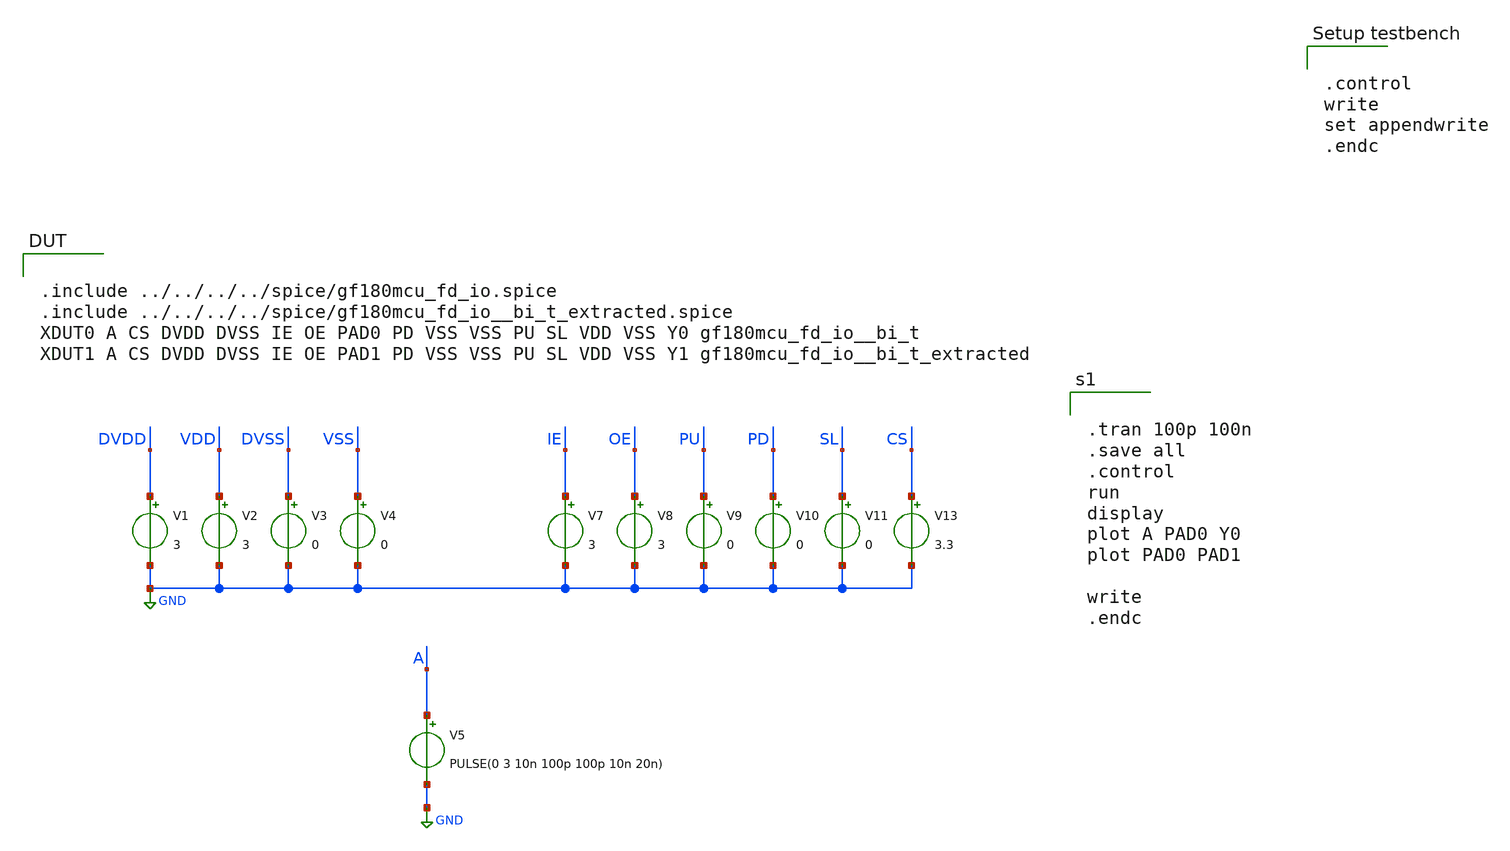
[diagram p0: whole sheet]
** sch_path: padframe/switching_bi_t_pex/test/switching_bi_t_pex.sch

.include $env(PDK_ROOT)/$env(PDK)/libs.tech/ngspice/design.ngspice
.lib $env(PDK_ROOT)/$env(PDK)/libs.tech/ngspice/sm141064.ngspice typical
.lib $env(PDK_ROOT)/$env(PDK)/libs.tech/ngspice/sm141064.ngspice diode_typical
.lib $env(PDK_ROOT)/$env(PDK)/libs.tech/ngspice/sm141064.ngspice res_typical
.lib $env(PDK_ROOT)/$env(PDK)/libs.tech/ngspice/sm141064.ngspice mimcap_typical
.lib $env(PDK_ROOT)/$env(PDK)/libs.tech/ngspice/sm141064.ngspice moscap_typical
.lib $env(PDK_ROOT)/$env(PDK)/libs.tech/ngspice/sm141064.ngspice bjt_typical
*.lib $env(PDK_ROOT)/$env(PDK)/libs.tech/ngspice/sm141064.ngspice cap_mim


.control
write
set appendwrite
.endc
**.subckt switching_bi_t_pex
V1 DVDD GND 3
V2 VDD GND 3
V3 DVSS GND 0
V4 VSS GND 0
V5 A GND PULSE(0 3 10n 100p 100p 10n 20n)
V7 IE GND 3
V8 OE GND 3
V9 PU GND 0
V10 PD GND 0
V11 SL GND 0
V13 CS GND 3.3
**** begin user architecture code


.tran 100p 100n
.save all
.control
run
display
plot A PAD0 Y0
plot PAD0 PAD1

write
.endc



.include ../../../../spice/gf180mcu_fd_io.spice
.include ../../../../spice/gf180mcu_fd_io__bi_t_extracted.spice
XDUT0 A CS DVDD DVSS IE OE PAD0 PD VSS VSS PU SL VDD VSS Y0 gf180mcu_fd_io__bi_t
XDUT1 A CS DVDD DVSS IE OE PAD1 PD VSS VSS PU SL VDD VSS Y1 gf180mcu_fd_io__bi_t_extracted

**** end user architecture code
**.ends
.GLOBAL GND
.end
